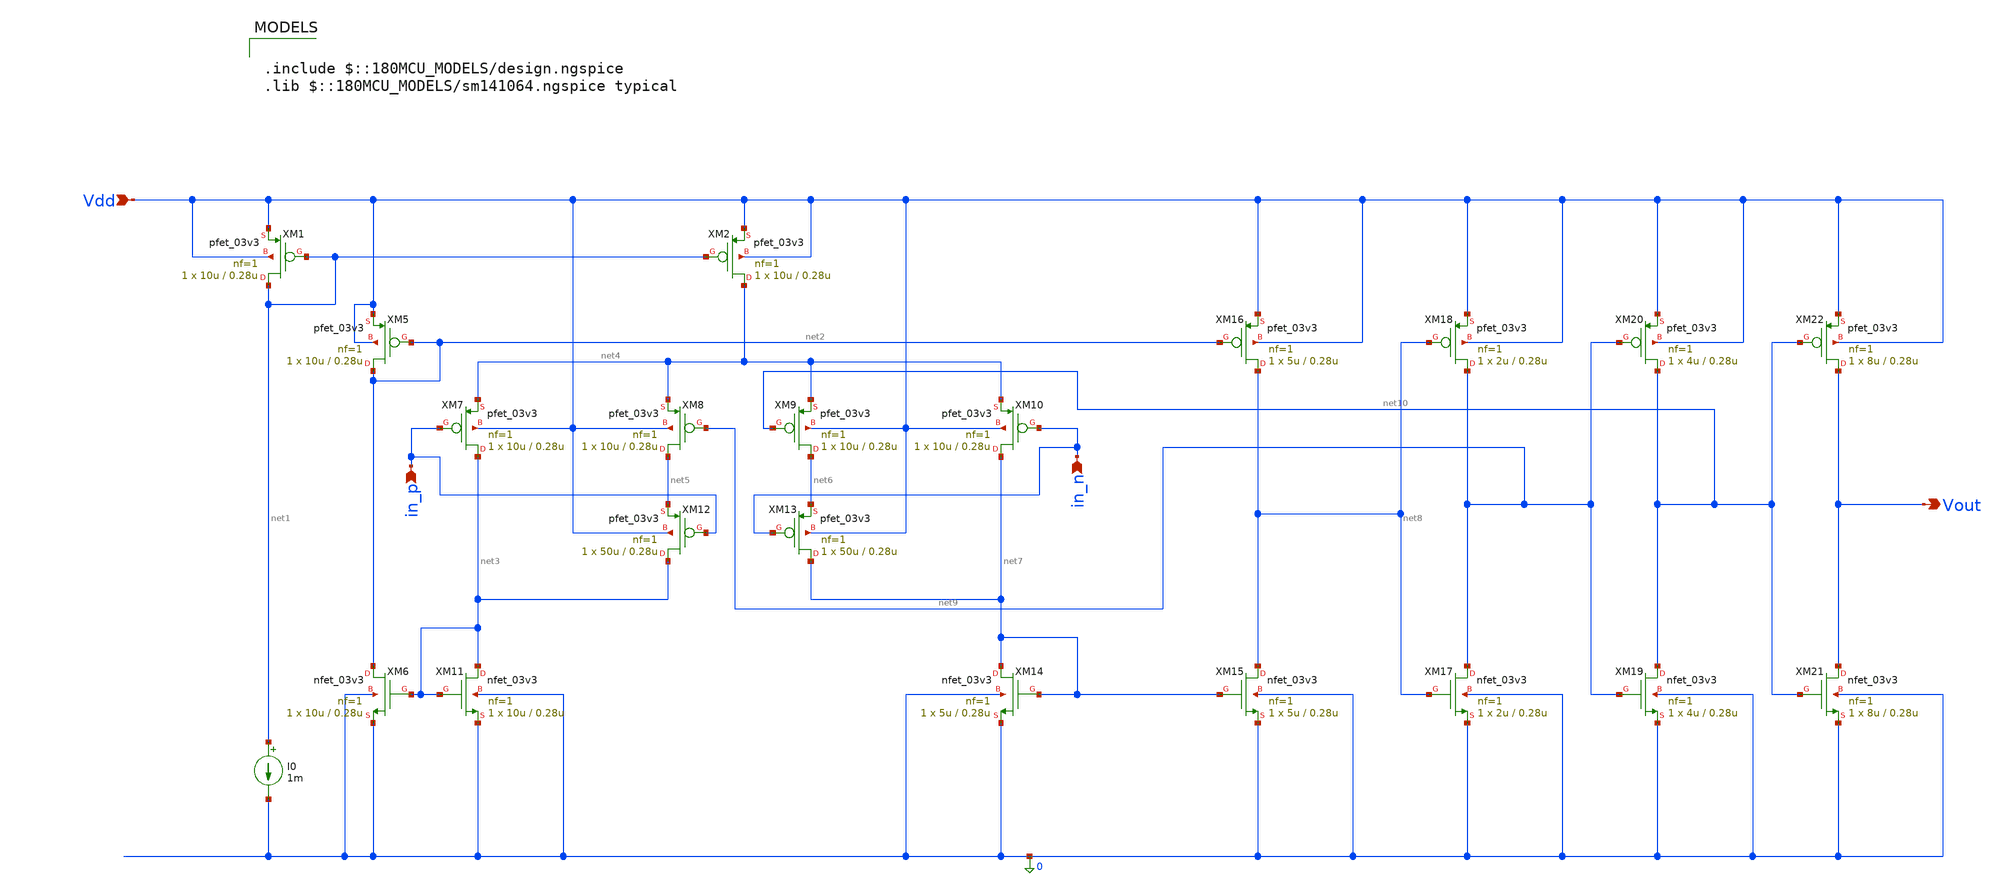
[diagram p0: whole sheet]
** sch_path: blocks/adc/lvds/lvds_rec_v1.sch
**.subckt lvds_rec_v1 Vdd in_n in_p Vout
*.ipin Vdd
*.ipin in_n
*.ipin in_p
*.opin Vout
XM1 net1 net1 Vdd Vdd pfet_03v3 L=0.28u W=10u nf=1 ad='int((nf+1)/2) * W/nf * 0.18u' as='int((nf+2)/2) * W/nf * 0.18u'
+ pd='2*int((nf+1)/2) * (W/nf + 0.18u)' ps='2*int((nf+2)/2) * (W/nf + 0.18u)' nrd='0.18u / W' nrs='0.18u / W'
+ sa=0 sb=0 sd=0 m=1
XM2 net4 net1 Vdd Vdd pfet_03v3 L=0.28u W=10u nf=1 ad='int((nf+1)/2) * W/nf * 0.18u' as='int((nf+2)/2) * W/nf * 0.18u'
+ pd='2*int((nf+1)/2) * (W/nf + 0.18u)' ps='2*int((nf+2)/2) * (W/nf + 0.18u)' nrd='0.18u / W' nrs='0.18u / W'
+ sa=0 sb=0 sd=0 m=1
XM5 net2 net2 Vdd Vdd pfet_03v3 L=0.28u W=10u nf=1 ad='int((nf+1)/2) * W/nf * 0.18u' as='int((nf+2)/2) * W/nf * 0.18u'
+ pd='2*int((nf+1)/2) * (W/nf + 0.18u)' ps='2*int((nf+2)/2) * (W/nf + 0.18u)' nrd='0.18u / W' nrs='0.18u / W'
+ sa=0 sb=0 sd=0 m=1
XM6 net2 net3 0 0 nfet_03v3 L=0.28u W=10u nf=1 ad='int((nf+1)/2) * W/nf * 0.18u' as='int((nf+2)/2) * W/nf * 0.18u'
+ pd='2*int((nf+1)/2) * (W/nf + 0.18u)' ps='2*int((nf+2)/2) * (W/nf + 0.18u)' nrd='0.18u / W' nrs='0.18u / W'
+ sa=0 sb=0 sd=0 m=1
XM7 net3 in_p net4 Vdd pfet_03v3 L=0.28u W=10u nf=1 ad='int((nf+1)/2) * W/nf * 0.18u' as='int((nf+2)/2) * W/nf * 0.18u'
+ pd='2*int((nf+1)/2) * (W/nf + 0.18u)' ps='2*int((nf+2)/2) * (W/nf + 0.18u)' nrd='0.18u / W' nrs='0.18u / W'
+ sa=0 sb=0 sd=0 m=1
XM8 net5 net9 net4 Vdd pfet_03v3 L=0.28u W=10u nf=1 ad='int((nf+1)/2) * W/nf * 0.18u' as='int((nf+2)/2) * W/nf * 0.18u'
+ pd='2*int((nf+1)/2) * (W/nf + 0.18u)' ps='2*int((nf+2)/2) * (W/nf + 0.18u)' nrd='0.18u / W' nrs='0.18u / W'
+ sa=0 sb=0 sd=0 m=1
XM9 net6 net10 net4 Vdd pfet_03v3 L=0.28u W=10u nf=1 ad='int((nf+1)/2) * W/nf * 0.18u' as='int((nf+2)/2) * W/nf * 0.18u'
+ pd='2*int((nf+1)/2) * (W/nf + 0.18u)' ps='2*int((nf+2)/2) * (W/nf + 0.18u)' nrd='0.18u / W' nrs='0.18u / W'
+ sa=0 sb=0 sd=0 m=1
XM10 net7 in_n net4 Vdd pfet_03v3 L=0.28u W=10u nf=1 ad='int((nf+1)/2) * W/nf * 0.18u' as='int((nf+2)/2) * W/nf * 0.18u'
+ pd='2*int((nf+1)/2) * (W/nf + 0.18u)' ps='2*int((nf+2)/2) * (W/nf + 0.18u)' nrd='0.18u / W' nrs='0.18u / W'
+ sa=0 sb=0 sd=0 m=1
XM11 net3 net3 0 0 nfet_03v3 L=0.28u W=10u nf=1 ad='int((nf+1)/2) * W/nf * 0.18u' as='int((nf+2)/2) * W/nf * 0.18u'
+ pd='2*int((nf+1)/2) * (W/nf + 0.18u)' ps='2*int((nf+2)/2) * (W/nf + 0.18u)' nrd='0.18u / W' nrs='0.18u / W'
+ sa=0 sb=0 sd=0 m=1
XM12 net3 in_p net5 Vdd pfet_03v3 L=0.28u W=50u nf=1 ad='int((nf+1)/2) * W/nf * 0.18u' as='int((nf+2)/2) * W/nf * 0.18u'
+ pd='2*int((nf+1)/2) * (W/nf + 0.18u)' ps='2*int((nf+2)/2) * (W/nf + 0.18u)' nrd='0.18u / W' nrs='0.18u / W'
+ sa=0 sb=0 sd=0 m=1
XM13 net7 in_n net6 Vdd pfet_03v3 L=0.28u W=50u nf=1 ad='int((nf+1)/2) * W/nf * 0.18u' as='int((nf+2)/2) * W/nf * 0.18u'
+ pd='2*int((nf+1)/2) * (W/nf + 0.18u)' ps='2*int((nf+2)/2) * (W/nf + 0.18u)' nrd='0.18u / W' nrs='0.18u / W'
+ sa=0 sb=0 sd=0 m=1
XM14 net7 net7 0 0 nfet_03v3 L=0.28u W=5u nf=1 ad='int((nf+1)/2) * W/nf * 0.18u' as='int((nf+2)/2) * W/nf * 0.18u'
+ pd='2*int((nf+1)/2) * (W/nf + 0.18u)' ps='2*int((nf+2)/2) * (W/nf + 0.18u)' nrd='0.18u / W' nrs='0.18u / W'
+ sa=0 sb=0 sd=0 m=1
XM15 net8 net7 0 0 nfet_03v3 L=0.28u W=5u nf=1 ad='int((nf+1)/2) * W/nf * 0.18u' as='int((nf+2)/2) * W/nf * 0.18u'
+ pd='2*int((nf+1)/2) * (W/nf + 0.18u)' ps='2*int((nf+2)/2) * (W/nf + 0.18u)' nrd='0.18u / W' nrs='0.18u / W'
+ sa=0 sb=0 sd=0 m=1
XM16 net8 net2 Vdd Vdd pfet_03v3 L=0.28u W=5u nf=1 ad='int((nf+1)/2) * W/nf * 0.18u' as='int((nf+2)/2) * W/nf * 0.18u'
+ pd='2*int((nf+1)/2) * (W/nf + 0.18u)' ps='2*int((nf+2)/2) * (W/nf + 0.18u)' nrd='0.18u / W' nrs='0.18u / W'
+ sa=0 sb=0 sd=0 m=1
XM17 net9 net8 0 0 nfet_03v3 L=0.28u W=2u nf=1 ad='int((nf+1)/2) * W/nf * 0.18u' as='int((nf+2)/2) * W/nf * 0.18u'
+ pd='2*int((nf+1)/2) * (W/nf + 0.18u)' ps='2*int((nf+2)/2) * (W/nf + 0.18u)' nrd='0.18u / W' nrs='0.18u / W'
+ sa=0 sb=0 sd=0 m=1
XM18 net9 net8 Vdd Vdd pfet_03v3 L=0.28u W=2u nf=1 ad='int((nf+1)/2) * W/nf * 0.18u' as='int((nf+2)/2) * W/nf * 0.18u'
+ pd='2*int((nf+1)/2) * (W/nf + 0.18u)' ps='2*int((nf+2)/2) * (W/nf + 0.18u)' nrd='0.18u / W' nrs='0.18u / W'
+ sa=0 sb=0 sd=0 m=1
XM19 net10 net9 0 0 nfet_03v3 L=0.28u W=4u nf=1 ad='int((nf+1)/2) * W/nf * 0.18u' as='int((nf+2)/2) * W/nf * 0.18u'
+ pd='2*int((nf+1)/2) * (W/nf + 0.18u)' ps='2*int((nf+2)/2) * (W/nf + 0.18u)' nrd='0.18u / W' nrs='0.18u / W'
+ sa=0 sb=0 sd=0 m=1
XM20 net10 net9 Vdd Vdd pfet_03v3 L=0.28u W=4u nf=1 ad='int((nf+1)/2) * W/nf * 0.18u' as='int((nf+2)/2) * W/nf * 0.18u'
+ pd='2*int((nf+1)/2) * (W/nf + 0.18u)' ps='2*int((nf+2)/2) * (W/nf + 0.18u)' nrd='0.18u / W' nrs='0.18u / W'
+ sa=0 sb=0 sd=0 m=1
XM21 Vout net10 0 0 nfet_03v3 L=0.28u W=8u nf=1 ad='int((nf+1)/2) * W/nf * 0.18u' as='int((nf+2)/2) * W/nf * 0.18u'
+ pd='2*int((nf+1)/2) * (W/nf + 0.18u)' ps='2*int((nf+2)/2) * (W/nf + 0.18u)' nrd='0.18u / W' nrs='0.18u / W'
+ sa=0 sb=0 sd=0 m=1
XM22 Vout net10 Vdd Vdd pfet_03v3 L=0.28u W=8u nf=1 ad='int((nf+1)/2) * W/nf * 0.18u' as='int((nf+2)/2) * W/nf * 0.18u'
+ pd='2*int((nf+1)/2) * (W/nf + 0.18u)' ps='2*int((nf+2)/2) * (W/nf + 0.18u)' nrd='0.18u / W' nrs='0.18u / W'
+ sa=0 sb=0 sd=0 m=1
I0 net1 0 1m
**** begin user architecture code

.include $::180MCU_MODELS/design.ngspice
.lib $::180MCU_MODELS/sm141064.ngspice typical

**** end user architecture code
**.ends
.end
